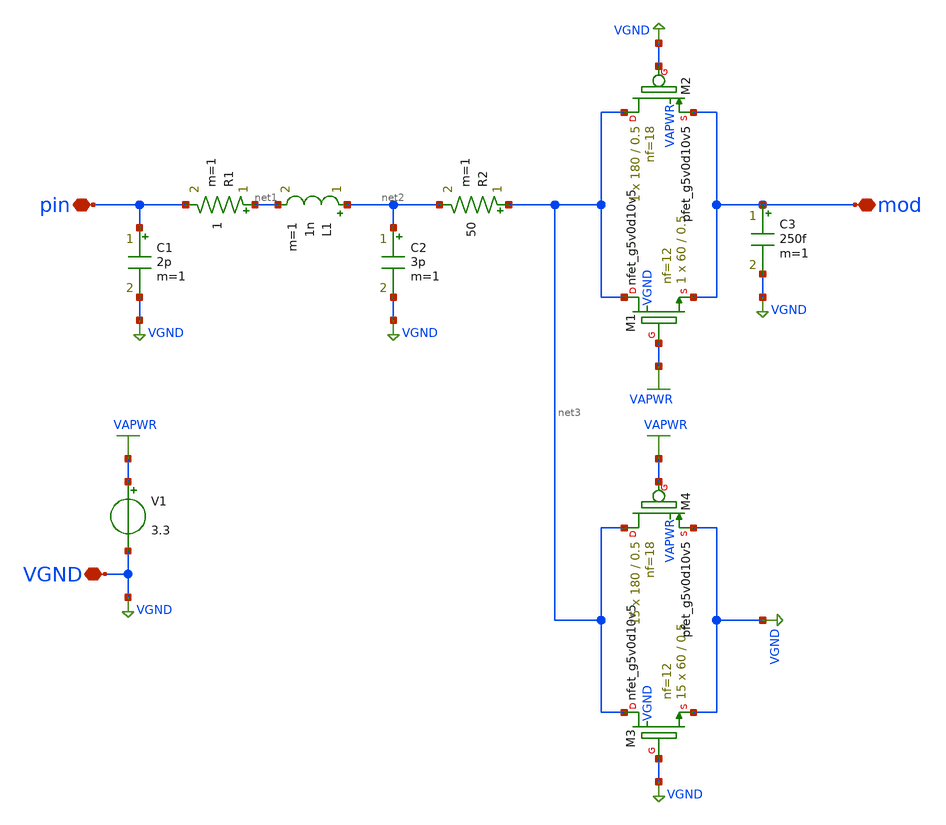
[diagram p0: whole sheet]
** sch_path: xschem/pad_model.sch
**.subckt pad_model pin mod VGND
*.iopin pin
*.iopin mod
*.iopin VGND
XM1 net3 VAPWR mod VGND sky130_fd_pr__nfet_g5v0d10v5 L=0.5 W=60 nf=12 ad='int((nf+1)/2) * W/nf * 0.29'
+ as='int((nf+2)/2) * W/nf * 0.29' pd='2*int((nf+1)/2) * (W/nf + 0.29)' ps='2*int((nf+2)/2) * (W/nf + 0.29)'
+ nrd='0.29 / W' nrs='0.29 / W' sa=0 sb=0 sd=0 mult=1 m=1
XM2 net3 VGND mod VAPWR sky130_fd_pr__pfet_g5v0d10v5 L=0.5 W=180 nf=18 ad='int((nf+1)/2) * W/nf * 0.29'
+ as='int((nf+2)/2) * W/nf * 0.29' pd='2*int((nf+1)/2) * (W/nf + 0.29)' ps='2*int((nf+2)/2) * (W/nf + 0.29)'
+ nrd='0.29 / W' nrs='0.29 / W' sa=0 sb=0 sd=0 mult=1 m=1
C1 pin VGND 2p m=1
V1 VAPWR VGND 3.3
R1 net1 pin 1 m=1
L1 net2 net1 1n m=1
C2 net2 VGND 3p m=1
R2 net3 net2 50 m=1
C3 mod VGND 250f m=1
XM3 net3 VGND VGND VGND sky130_fd_pr__nfet_g5v0d10v5 L=0.5 W=60 nf=12 ad='int((nf+1)/2) * W/nf * 0.29'
+ as='int((nf+2)/2) * W/nf * 0.29' pd='2*int((nf+1)/2) * (W/nf + 0.29)' ps='2*int((nf+2)/2) * (W/nf + 0.29)'
+ nrd='0.29 / W' nrs='0.29 / W' sa=0 sb=0 sd=0 mult=15 m=15
XM4 net3 VAPWR VGND VAPWR sky130_fd_pr__pfet_g5v0d10v5 L=0.5 W=180 nf=18 ad='int((nf+1)/2) * W/nf * 0.29'
+ as='int((nf+2)/2) * W/nf * 0.29' pd='2*int((nf+1)/2) * (W/nf + 0.29)' ps='2*int((nf+2)/2) * (W/nf + 0.29)'
+ nrd='0.29 / W' nrs='0.29 / W' sa=0 sb=0 sd=0 mult=15 m=15
**.ends
.end
